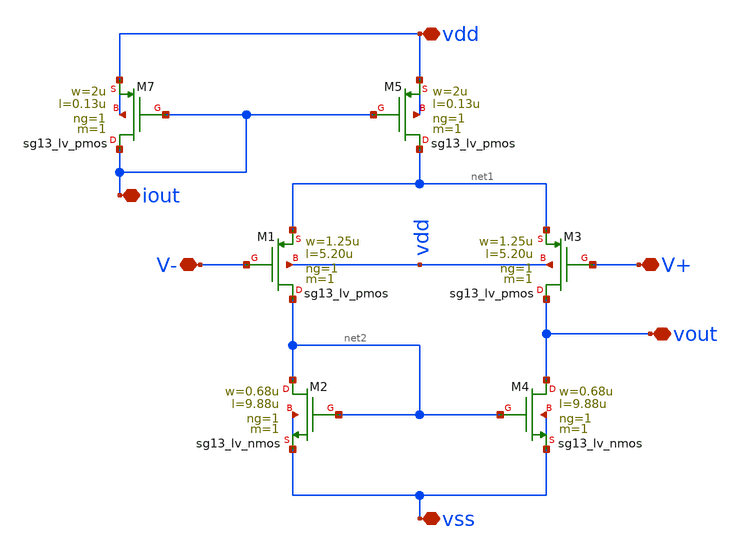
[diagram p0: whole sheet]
** sch_path: utils/gmid_demonstration/testbench/schematic.sch
**.subckt schematic vdd iout vout vss V+ V-
*.iopin vdd
*.iopin iout
*.iopin vout
*.iopin vss
*.iopin V+
*.iopin V-
XM1 net2 V- net1 vdd sg13_lv_pmos w=1.25u l=5.20u ng=1 m=1 mm_ok=1
XM2 net2 net2 vss vss sg13_lv_nmos w=0.68u l=9.88u ng=1 m=1 mm_ok=1
XM3 vout V+ net1 vdd sg13_lv_pmos w=1.25u l=5.20u ng=1 m=1 mm_ok=1
XM4 vout net2 vss vss sg13_lv_nmos w=0.68u l=9.88u ng=1 m=1 mm_ok=1
XM5 net1 iout vdd vdd sg13_lv_pmos w=2u l=0.13u ng=1 m=1 mm_ok=1
XM7 iout iout vdd vdd sg13_lv_pmos w=2u l=0.13u ng=1 m=1 mm_ok=1
**.ends
.end
